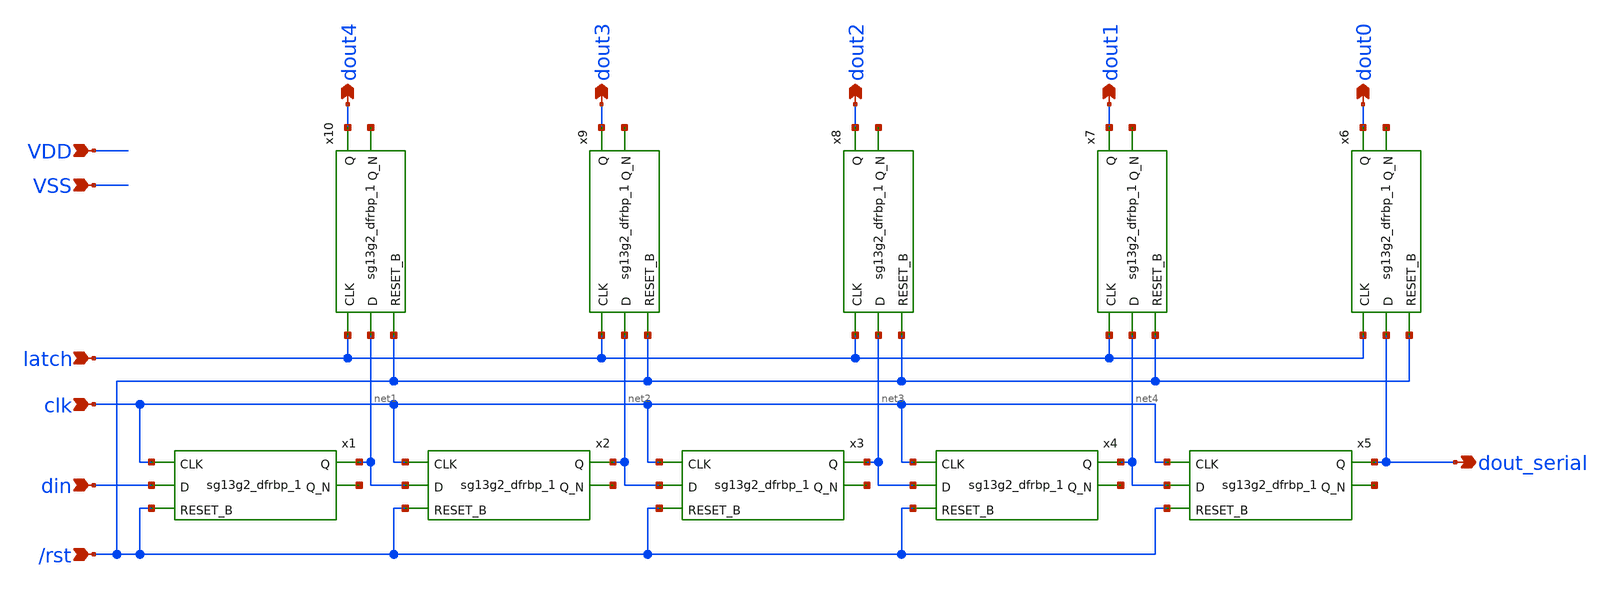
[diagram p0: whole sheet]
** sch_path: xschem/digital/shift_reg.sch
**.subckt shift_reg din /rst clk dout3 dout0 dout1 dout2 dout4 latch VDD VSS dout_serial
*.ipin din
*.ipin /rst
*.ipin clk
*.opin dout3
*.opin dout0
*.opin dout1
*.opin dout2
*.opin dout4
*.ipin latch
*.ipin VDD
*.ipin VSS
*.opin dout_serial
x1 net1 net5 clk din /rst VDD VSS sg13g2_dfrbp_1
x2 net2 net6 clk net1 /rst VDD VSS sg13g2_dfrbp_1
x3 net3 net7 clk net2 /rst VDD VSS sg13g2_dfrbp_1
x4 net4 net8 clk net3 /rst VDD VSS sg13g2_dfrbp_1
x5 dout_serial net9 clk net4 /rst VDD VSS sg13g2_dfrbp_1
x6 dout0 net10 latch dout_serial /rst VDD VSS sg13g2_dfrbp_1
x7 dout1 net11 latch net4 /rst VDD VSS sg13g2_dfrbp_1
x8 dout2 net12 latch net3 /rst VDD VSS sg13g2_dfrbp_1
x9 dout3 net13 latch net2 /rst VDD VSS sg13g2_dfrbp_1
x10 dout4 net14 latch net1 /rst VDD VSS sg13g2_dfrbp_1
**.ends

* expanding   symbol:  sg13g2_stdcells/sg13g2_dfrbp_1.sym # of pins=5
** sym_path: sg13g2_stdcells/sg13g2_dfrbp_1.sym
** sch_path: sg13g2_stdcells/sg13g2_dfrbp_1.sch
.subckt sg13g2_dfrbp_1 Q Q_N CLK D RESET_B VDD VSS
*.ipin D
*.ipin RESET_B
*.ipin CLK
*.opin Q
*.opin Q_N
*.iopin VDD
*.iopin VSS
XM1 Db D net10 VSS sg13_lv_nmos w=420.00n l=130.00n ng=1 m=1 mm_ok=1
XM2 net10 RESET_B VSS VSS sg13_lv_nmos w=420.00n l=130.00n ng=1 m=1 mm_ok=1
XM3 net1 clkneg net9 VSS sg13_lv_nmos w=420.00n l=130.00n ng=1 m=1 mm_ok=1
XM4 net9 net1 VSS VSS sg13_lv_nmos w=420.00n l=130.00n ng=1 m=1 mm_ok=1
XM5 net1 net1 net5 VSS sg13_lv_nmos w=420.00n l=130.00n ng=1 m=1 mm_ok=1
XM6 net5 RESET_B VSS VSS sg13_lv_nmos w=420.00n l=130.00n ng=1 m=1 mm_ok=1
XM7 Q_N net1 VSS VSS sg13_lv_nmos w=740.00n l=130.00n ng=1 m=1 mm_ok=1
XM8 net2 net1 VSS VSS sg13_lv_nmos w=740.00n l=130.00n ng=1 m=1 mm_ok=1
XM9 Q net2 VSS VSS sg13_lv_nmos w=740.00n l=130.00n ng=1 m=1 mm_ok=1
XM10 clkneg CLK VSS VSS sg13_lv_nmos w=740.00n l=130.00n ng=1 m=1 mm_ok=1
XM11 clkpos clkneg VSS VSS sg13_lv_nmos w=740.00n l=130.00n ng=1 m=1 mm_ok=1
XM12 Db clkneg net3 VSS sg13_lv_nmos w=420.00n l=130.00n ng=1 m=1 mm_ok=1
XM13 net3 clkpos net8 VSS sg13_lv_nmos w=420.00n l=130.00n ng=1 m=1 mm_ok=1
XM14 net8 net3 net4 VSS sg13_lv_nmos w=420.00n l=130.00n ng=1 m=1 mm_ok=1
XM15 net4 RESET_B VSS VSS sg13_lv_nmos w=420.00n l=130.00n ng=1 m=1 mm_ok=1
XM16 net3 net3 VSS VSS sg13_lv_nmos w=740.00n l=130.00n ng=1 m=1 mm_ok=1
XM17 net3 clkpos net1 VSS sg13_lv_nmos w=740.00n l=130.00n ng=1 m=1 mm_ok=1
XM18 Db RESET_B VDD VDD sg13_lv_pmos w=420.00n l=130.00n ng=1 m=1 mm_ok=1
XM19 Db D VDD VDD sg13_lv_pmos w=420.00n l=130.00n ng=1 m=1 mm_ok=1
XM20 net7 net1 VDD VDD sg13_lv_pmos w=420.00n l=130.00n ng=1 m=1 mm_ok=1
XM21 net1 clkpos net7 VDD sg13_lv_pmos w=420.00n l=130.00n ng=1 m=1 mm_ok=1
XM22 net1 net1 VDD VDD sg13_lv_pmos w=420.00n l=130.00n ng=1 m=1 mm_ok=1
XM23 net1 RESET_B VDD VDD sg13_lv_pmos w=420.00n l=130.00n ng=1 m=1 mm_ok=1
XM24 Q_N net1 VDD VDD sg13_lv_pmos w=1.12u l=130.00n ng=1 m=1 mm_ok=1
XM25 net2 net1 VDD VDD sg13_lv_pmos w=1.12u l=130.00n ng=1 m=1 mm_ok=1
XM26 Q net2 VDD VDD sg13_lv_pmos w=1.12u l=130.00n ng=1 m=1 mm_ok=1
XM27 clkneg CLK VDD VDD sg13_lv_pmos w=1.12u l=130.00n ng=1 m=1 mm_ok=1
XM28 clkpos clkneg VDD VDD sg13_lv_pmos w=1.12u l=130.00n ng=1 m=1 mm_ok=1
XM29 Db clkpos net3 VDD sg13_lv_pmos w=420.00n l=130.00n ng=1 m=1 mm_ok=1
XM30 net6 net3 VDD VDD sg13_lv_pmos w=420.00n l=130.00n ng=1 m=1 mm_ok=1
XM31 net3 clkneg net6 VDD sg13_lv_pmos w=420.00n l=130.00n ng=1 m=1 mm_ok=1
XM32 net3 RESET_B VDD VDD sg13_lv_pmos w=420.00n l=130.00n ng=1 m=1 mm_ok=1
XM33 net3 net3 VDD VDD sg13_lv_pmos w=1.000u l=130.00n ng=1 m=1 mm_ok=1
XM34 net3 clkneg net1 VDD sg13_lv_pmos w=1.000u l=130.00n ng=1 m=1 mm_ok=1
.ends

.end
